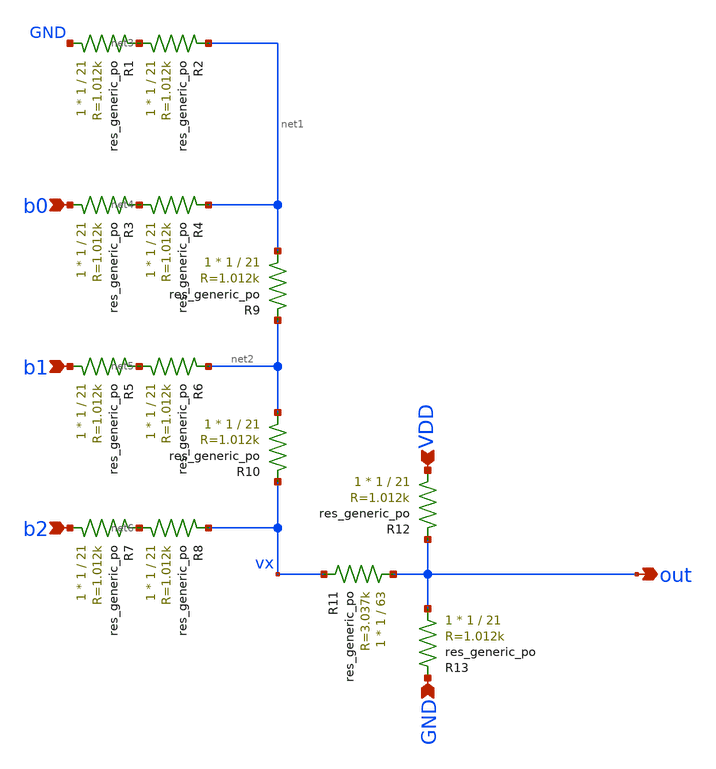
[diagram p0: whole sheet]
** sch_path: xschem/DAC3bit.sch
**.subckt DAC3bit out b0 b1 b2 GND VDD
*.opin out
*.ipin b0
*.ipin b1
*.ipin b2
*.ipin GND
*.ipin VDD
XR1 GND net3 sky130_fd_pr__res_generic_po W=1 L=21 m=1
XR2 net3 net1 sky130_fd_pr__res_generic_po W=1 L=21 m=1
XR3 b0 net4 sky130_fd_pr__res_generic_po W=1 L=21 m=1
XR4 net4 net1 sky130_fd_pr__res_generic_po W=1 L=21 m=1
XR5 b1 net5 sky130_fd_pr__res_generic_po W=1 L=21 m=1
XR6 net5 net2 sky130_fd_pr__res_generic_po W=1 L=21 m=1
XR7 b2 net6 sky130_fd_pr__res_generic_po W=1 L=21 m=1
XR8 net6 vx sky130_fd_pr__res_generic_po W=1 L=21 m=1
XR9 net1 net2 sky130_fd_pr__res_generic_po W=1 L=21 m=1
XR10 net2 vx sky130_fd_pr__res_generic_po W=1 L=21 m=1
XR12 VDD out sky130_fd_pr__res_generic_po W=1 L=21 m=1
XR13 out GND sky130_fd_pr__res_generic_po W=1 L=21 m=1
XR11 out vx sky130_fd_pr__res_generic_po W=1 L=63 m=1
**.ends
.end
